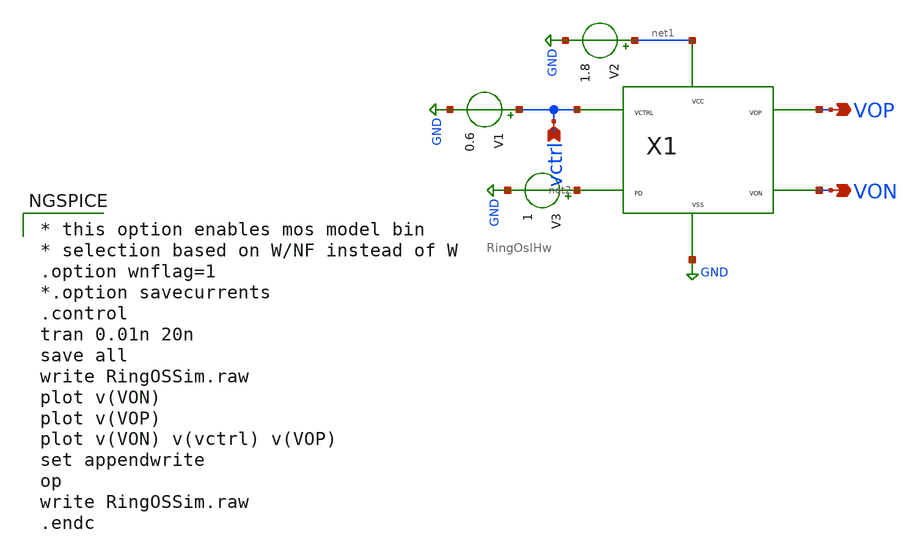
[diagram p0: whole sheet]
** sch_path: xschem/RingOSSim.sch
**.subckt RingOSSim VOP VON vctrl
*.opin VOP
*.opin VON
*.ipin vctrl
X1 vctrl net2 VOP VON net1 GND RingOslHw
V2 net1 GND 1.8
V3 net2 GND 1
V1 vctrl GND 0.6
**** begin user architecture code

** opencircuitdesign pdks install
.lib $::SKYWATER_MODELS/sky130.lib.spice tt



* this option enables mos model bin
* selection based on W/NF instead of W
.option wnflag=1
*.option savecurrents
.control
tran 0.01n 20n
save all
write RingOSSim.raw
plot v(VON)
plot v(VOP)
plot v(VON) v(vctrl) v(VOP)
set appendwrite
op
write RingOSSim.raw
.endc


**** end user architecture code
**.ends

* expanding   symbol:  RingOslHw.sym # of pins=6
** sym_path: xschem/RingOslHw.sym
** sch_path: xschem/RingOslHw.sch
.subckt RingOslHw VCTRL PD VOP VON VCC VSS
*.ipin PD
*.ipin VCTRL
*.iopin VCC
*.iopin VSS
*.opin VON
*.opin VOP
X2 VCC VSS net4 net3 VCTRL PD VOP VON inverterblock
X1 VCC VSS net2 net1 VCTRL PD net3 net4 inverterblock
X3 VCC VSS VON VOP VCTRL PD net1 net2 inverterblock
.ends


* expanding   symbol:  inverterblock.sym # of pins=16
** sym_path: xschem/inverterblock.sym
** sch_path: xschem/inverterblock.sch
.subckt inverterblock VCC VSS VON VOP VCTRL PD VIN VIP
*.ipin VIP
*.opin VON
*.opin VOP
*.ipin PD
*.iopin VSS
*.ipin VIN
*.ipin VCTRL
*.iopin VCC
*.ipin VCTRL
XM9 net1 PD VSS VSS sky130_fd_pr__nfet_01v8 L=0.15 W=1 nf=1 ad='int((nf+1)/2) * W/nf * 0.29' as='int((nf+2)/2) * W/nf * 0.29'
+ pd='2*int((nf+1)/2) * (W/nf + 0.29)' ps='2*int((nf+2)/2) * (W/nf + 0.29)' nrd='0.29 / W' nrs='0.29 / W'
+ sa=0 sb=0 sd=0 mult=1 m=1
XM10 VON VCTRL VCC VCC sky130_fd_pr__pfet_01v8 L=0.15 W=1 nf=1 ad='int((nf+1)/2) * W/nf * 0.29' as='int((nf+2)/2) * W/nf * 0.29'
+ pd='2*int((nf+1)/2) * (W/nf + 0.29)' ps='2*int((nf+2)/2) * (W/nf + 0.29)' nrd='0.29 / W' nrs='0.29 / W'
+ sa=0 sb=0 sd=0 mult=1 m=1
XM3 VON VOP VCC VCC sky130_fd_pr__pfet_01v8 L=0.15 W=1 nf=1 ad='int((nf+1)/2) * W/nf * 0.29' as='int((nf+2)/2) * W/nf * 0.29'
+ pd='2*int((nf+1)/2) * (W/nf + 0.29)' ps='2*int((nf+2)/2) * (W/nf + 0.29)' nrd='0.29 / W' nrs='0.29 / W'
+ sa=0 sb=0 sd=0 mult=1 m=1
XM4 VOP VON VCC VCC sky130_fd_pr__pfet_01v8 L=0.15 W=1 nf=1 ad='int((nf+1)/2) * W/nf * 0.29' as='int((nf+2)/2) * W/nf * 0.29'
+ pd='2*int((nf+1)/2) * (W/nf + 0.29)' ps='2*int((nf+2)/2) * (W/nf + 0.29)' nrd='0.29 / W' nrs='0.29 / W'
+ sa=0 sb=0 sd=0 mult=1 m=1
XM5 VOP VCTRL VCC VCC sky130_fd_pr__pfet_01v8 L=0.15 W=1 nf=1 ad='int((nf+1)/2) * W/nf * 0.29' as='int((nf+2)/2) * W/nf * 0.29'
+ pd='2*int((nf+1)/2) * (W/nf + 0.29)' ps='2*int((nf+2)/2) * (W/nf + 0.29)' nrd='0.29 / W' nrs='0.29 / W'
+ sa=0 sb=0 sd=0 mult=1 m=1
XM6 VON VIP net1 VSS sky130_fd_pr__nfet_01v8 L=0.15 W=1 nf=1 ad='int((nf+1)/2) * W/nf * 0.29' as='int((nf+2)/2) * W/nf * 0.29'
+ pd='2*int((nf+1)/2) * (W/nf + 0.29)' ps='2*int((nf+2)/2) * (W/nf + 0.29)' nrd='0.29 / W' nrs='0.29 / W'
+ sa=0 sb=0 sd=0 mult=1 m=1
XM7 VOP VIN net1 VSS sky130_fd_pr__nfet_01v8 L=0.15 W=1 nf=1 ad='int((nf+1)/2) * W/nf * 0.29' as='int((nf+2)/2) * W/nf * 0.29'
+ pd='2*int((nf+1)/2) * (W/nf + 0.29)' ps='2*int((nf+2)/2) * (W/nf + 0.29)' nrd='0.29 / W' nrs='0.29 / W'
+ sa=0 sb=0 sd=0 mult=1 m=1
.ends

.GLOBAL GND
.end
